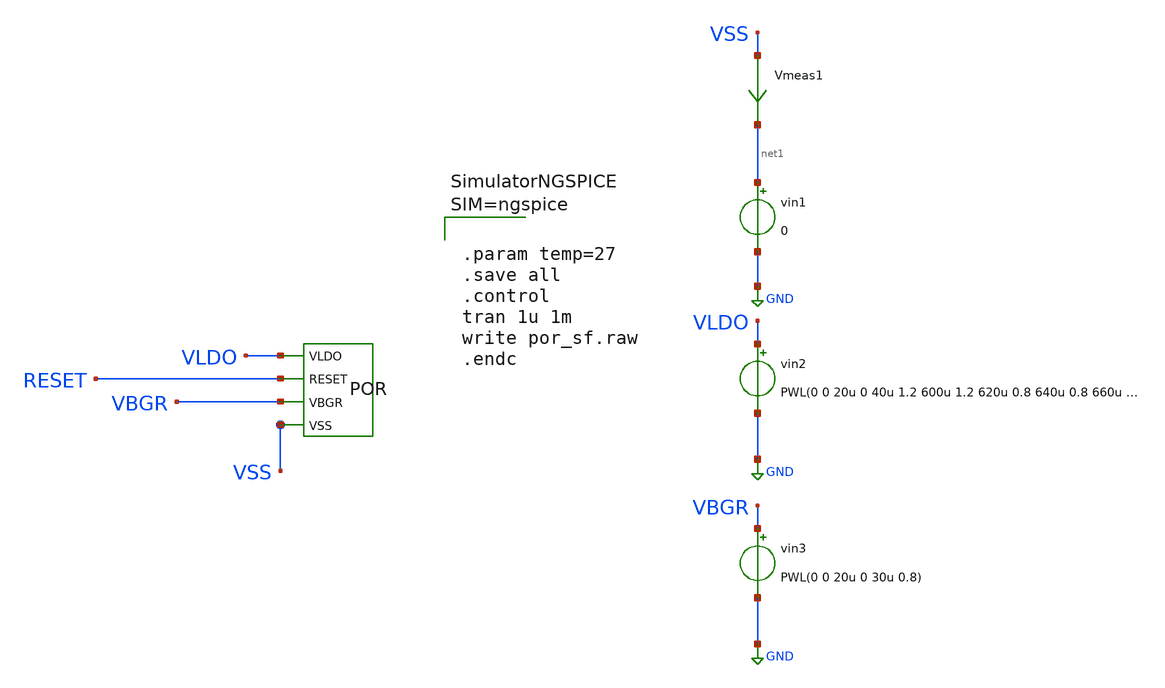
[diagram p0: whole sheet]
** sch_path: dependencies/POR/POR-main/testbenches/corners/xschem/por_post_layout_sim_fs.sch
**.subckt por_post_layout_sim_fs
X1 VLDO RESET VBGR VSS POR
vin1 net1 GND 0
Vmeas1 VSS net1 0
.save i(vmeas1)
vin2 VLDO GND PWL(0 0 20u 0 40u 1.2 600u 1.2 620u 0.8 640u 0.8 660u 1.2 760u 1.2 780u 0)
vin3 VBGR GND PWL(0 0 20u 0 30u 0.8)
**** begin user architecture code



.param temp=27
.save all
.control
tran 1u 1m
write por_sf.raw
.endc






.include /foss/designs/simulations/POR/output/POR__POR/magic_RC/POR.pex.spice
.lib cornerMOSlv.lib mos_fs
.lib cornerMOShv.lib mos_fs
.lib cornerHBT.lib hbt_typ
.lib cornerRES.lib res_typ
.lib cornerDIO.lib dio_tt
.lib cornerCAP.lib cap_typ



**** end user architecture code
**.ends
.GLOBAL GND
.end
